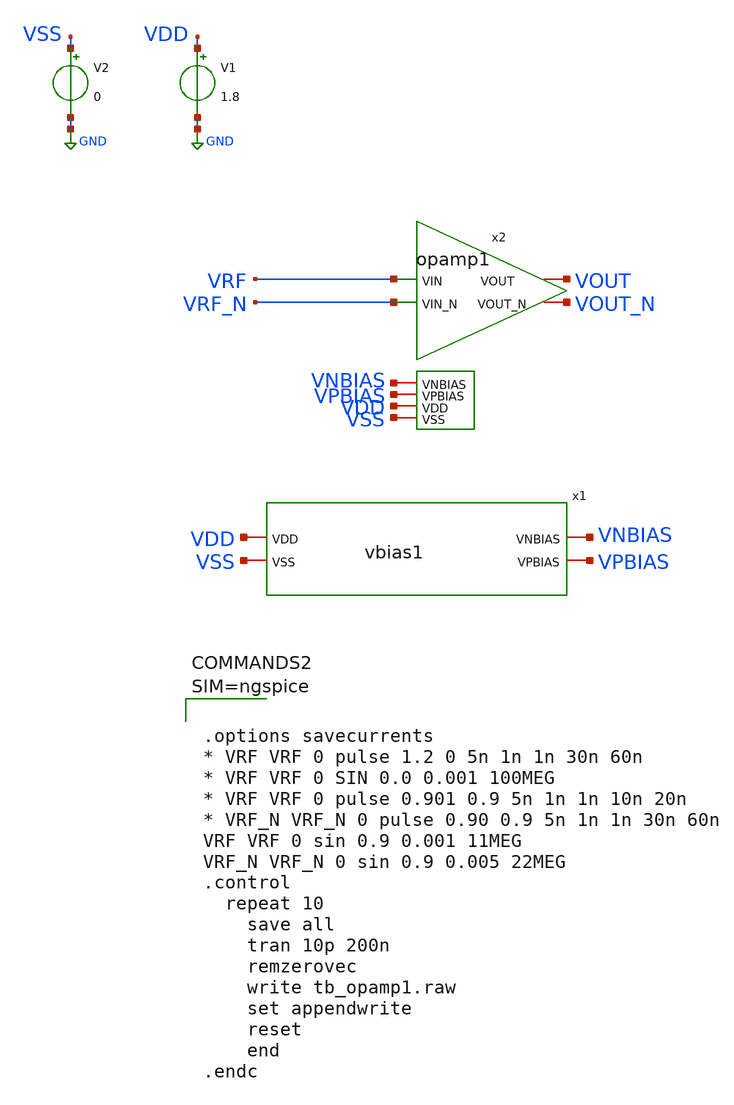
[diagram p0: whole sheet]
** sch_path: tt_um_emilian_rf_playground/xschem/tb_opamp1.sch
**.subckt tb_opamp1
x1 VDD VSS VPBIAS VNBIAS vbias1
x2 VDD VRF VRF_N VNBIAS VOUT VOUT_N VPBIAS VSS opamp1
V1 VDD GND 1.8
V2 VSS GND 0
**** begin user architecture code

** opencircuitdesign pdks install
.lib $::SKYWATER_MODELS/sky130.lib.spice tt_mm





.options savecurrents
* VRF VRF 0 pulse 1.2 0 5n 1n 1n 30n 60n
* VRF VRF 0 SIN 0.0 0.001 100MEG
* VRF VRF 0 pulse 0.901 0.9 5n 1n 1n 10n 20n
* VRF_N VRF_N 0 pulse 0.90 0.9 5n 1n 1n 30n 60n
VRF VRF 0 sin 0.9 0.001 11MEG
VRF_N VRF_N 0 sin 0.9 0.005 22MEG
.control
  repeat 10
    save all
    tran 10p 200n
    remzerovec
    write tb_opamp1.raw
    set appendwrite
    reset
    end
.endc



**** end user architecture code
**.ends

* expanding   symbol:  vbias1.sym # of pins=4
** sym_path: tt_um_emilian_rf_playground/xschem/vbias1.sym
** sch_path: tt_um_emilian_rf_playground/xschem/vbias1.sch
.subckt vbias1 VDD VSS VPBIAS VNBIAS
*.iopin VDD
*.iopin VSS
*.iopin VPBIAS
*.iopin VNBIAS
XR1 net2 VDD VSS sky130_fd_pr__res_high_po W=0.35 L=3 mult=1 m=1
XM8 VPBIAS VPBIAS VDD VDD sky130_fd_pr__pfet_01v8 L=1 W=8 nf=1 ad='int((nf+1)/2) * W/nf * 0.29' as='int((nf+2)/2) * W/nf * 0.29'
+ pd='2*int((nf+1)/2) * (W/nf + 0.29)' ps='2*int((nf+2)/2) * (W/nf + 0.29)' nrd='0.29 / W' nrs='0.29 / W'
+ sa=0 sb=0 sd=0 mult=1 m=1
vnbias net2 VNBIAS 0
.save i(vnbias)
vpbias VPBIAS net1 0
.save i(vpbias)
XM1 VNBIAS VNBIAS VSS VSS sky130_fd_pr__nfet_01v8 L=1 W=4 nf=1 ad='int((nf+1)/2) * W/nf * 0.29' as='int((nf+2)/2) * W/nf * 0.29'
+ pd='2*int((nf+1)/2) * (W/nf + 0.29)' ps='2*int((nf+2)/2) * (W/nf + 0.29)' nrd='0.29 / W' nrs='0.29 / W'
+ sa=0 sb=0 sd=0 mult=1 m=1
XM2 net1 VNBIAS VSS VSS sky130_fd_pr__nfet_01v8 L=1 W=4 nf=1 ad='int((nf+1)/2) * W/nf * 0.29' as='int((nf+2)/2) * W/nf * 0.29'
+ pd='2*int((nf+1)/2) * (W/nf + 0.29)' ps='2*int((nf+2)/2) * (W/nf + 0.29)' nrd='0.29 / W' nrs='0.29 / W'
+ sa=0 sb=0 sd=0 mult=1 m=1
.ends


* expanding   symbol:  opamp1.sym # of pins=8
** sym_path: tt_um_emilian_rf_playground/xschem/opamp1.sym
** sch_path: tt_um_emilian_rf_playground/xschem/opamp1.sch
.subckt opamp1 VDD VIN VIN_N VNBIAS VOUT VOUT_N VPBIAS VSS
*.ipin VIN
*.ipin VIN_N
*.iopin VOUT
*.iopin VOUT_N
*.iopin VPBIAS
*.iopin VNBIAS
*.iopin VDD
*.iopin VSS
XM5 VOUT_N VIN vcom VSS sky130_fd_pr__nfet_01v8_lvt L=1 W=32 nf=1 ad='int((nf+1)/2) * W/nf * 0.29' as='int((nf+2)/2) * W/nf * 0.29'
+ pd='2*int((nf+1)/2) * (W/nf + 0.29)' ps='2*int((nf+2)/2) * (W/nf + 0.29)' nrd='0.29 / W' nrs='0.29 / W'
+ sa=0 sb=0 sd=0 mult=1 m=1
vbiasp1 net2 VOUT_N 0
.save i(vbiasp1)
XM2 net3 VPBIAS VDD VDD sky130_fd_pr__pfet_01v8 L=1 W=8 nf=1 ad='int((nf+1)/2) * W/nf * 0.29' as='int((nf+2)/2) * W/nf * 0.29'
+ pd='2*int((nf+1)/2) * (W/nf + 0.29)' ps='2*int((nf+2)/2) * (W/nf + 0.29)' nrd='0.29 / W' nrs='0.29 / W'
+ sa=0 sb=0 sd=0 mult=1 m=1
vbiasp2 net3 VOUT 0
.save i(vbiasp2)
vbiasn vcom net1 0
.save i(vbiasn)
XM7 net1 VNBIAS VSS VSS sky130_fd_pr__nfet_01v8_lvt L=1 W=4 nf=1 ad='int((nf+1)/2) * W/nf * 0.29' as='int((nf+2)/2) * W/nf * 0.29'
+ pd='2*int((nf+1)/2) * (W/nf + 0.29)' ps='2*int((nf+2)/2) * (W/nf + 0.29)' nrd='0.29 / W' nrs='0.29 / W'
+ sa=0 sb=0 sd=0 mult=1 m=1
XM6 VOUT VIN_N vcom VSS sky130_fd_pr__nfet_01v8_lvt L=1 W=32 nf=1 ad='int((nf+1)/2) * W/nf * 0.29' as='int((nf+2)/2) * W/nf * 0.29'
+ pd='2*int((nf+1)/2) * (W/nf + 0.29)' ps='2*int((nf+2)/2) * (W/nf + 0.29)' nrd='0.29 / W' nrs='0.29 / W'
+ sa=0 sb=0 sd=0 mult=1 m=1
XM9 net2 VPBIAS VDD VDD sky130_fd_pr__pfet_01v8 L=1 W=8 nf=1 ad='int((nf+1)/2) * W/nf * 0.29' as='int((nf+2)/2) * W/nf * 0.29'
+ pd='2*int((nf+1)/2) * (W/nf + 0.29)' ps='2*int((nf+2)/2) * (W/nf + 0.29)' nrd='0.29 / W' nrs='0.29 / W'
+ sa=0 sb=0 sd=0 mult=1 m=1
.ends

.GLOBAL GND
.end
